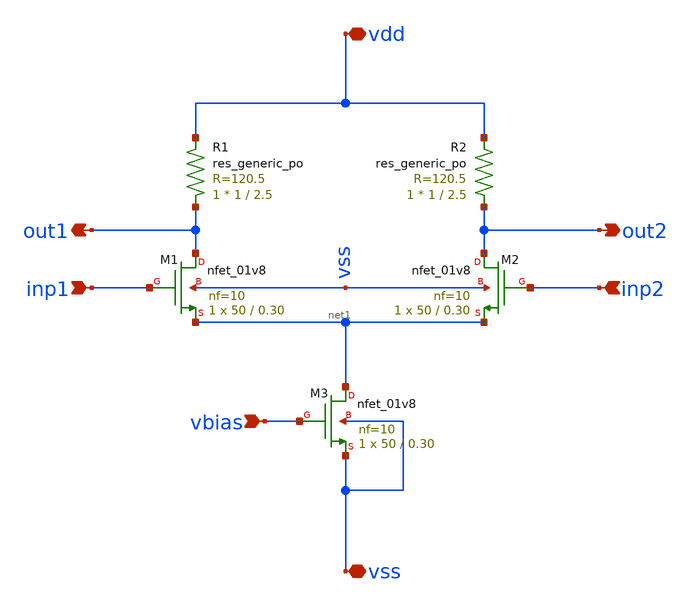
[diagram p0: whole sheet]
** sch_path: xschem/Diffamp.sch
**.subckt Diffamp vdd vss inp1 inp2 out2 out1 vbias
*.iopin vdd
*.iopin vss
*.ipin inp1
*.ipin inp2
*.opin out2
*.opin out1
*.ipin vbias
XM1 out1 inp1 net1 vss sky130_fd_pr__nfet_01v8 L=0.30 W=50 nf=10 ad='int((nf+1)/2) * W/nf * 0.29' as='int((nf+2)/2) * W/nf * 0.29'
+ pd='2*int((nf+1)/2) * (W/nf + 0.29)' ps='2*int((nf+2)/2) * (W/nf + 0.29)' nrd='0.29 / W' nrs='0.29 / W'
+ sa=0 sb=0 sd=0 mult=1 m=1
XM2 out2 inp2 net1 vss sky130_fd_pr__nfet_01v8 L=0.30 W=50 nf=10 ad='int((nf+1)/2) * W/nf * 0.29' as='int((nf+2)/2) * W/nf * 0.29'
+ pd='2*int((nf+1)/2) * (W/nf + 0.29)' ps='2*int((nf+2)/2) * (W/nf + 0.29)' nrd='0.29 / W' nrs='0.29 / W'
+ sa=0 sb=0 sd=0 mult=1 m=1
XR1 out1 vdd sky130_fd_pr__res_generic_po W=1 L=2.5 m=1
XR2 out2 vdd sky130_fd_pr__res_generic_po W=1 L=2.5 m=1
XM3 net1 vbias vss vss sky130_fd_pr__nfet_01v8 L=0.30 W=50 nf=10 ad='int((nf+1)/2) * W/nf * 0.29' as='int((nf+2)/2) * W/nf * 0.29'
+ pd='2*int((nf+1)/2) * (W/nf + 0.29)' ps='2*int((nf+2)/2) * (W/nf + 0.29)' nrd='0.29 / W' nrs='0.29 / W'
+ sa=0 sb=0 sd=0 mult=1 m=1
**.ends
.end
